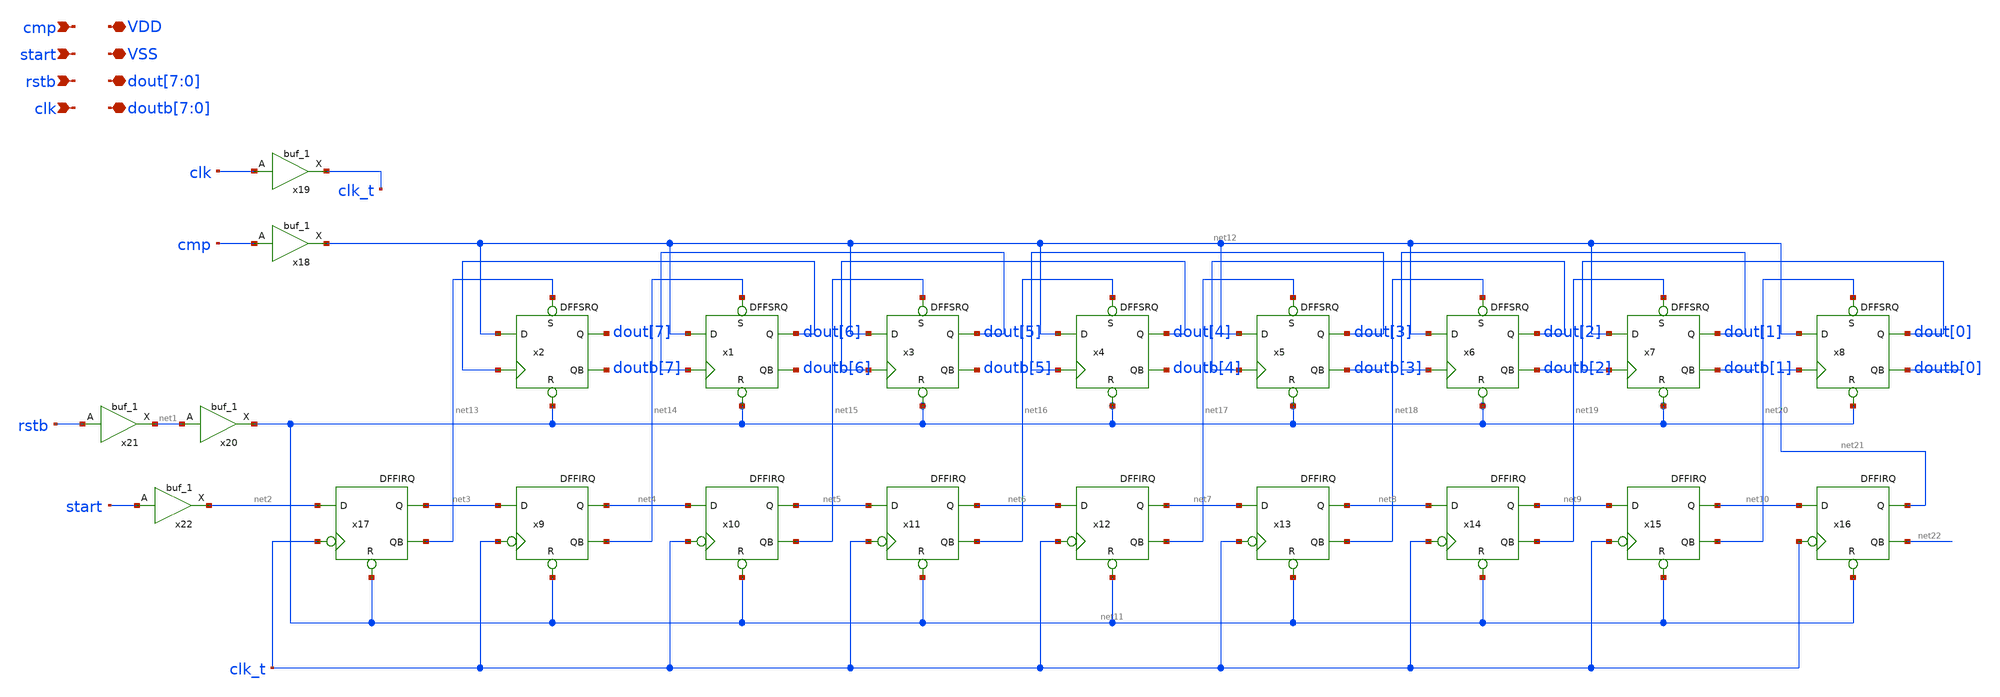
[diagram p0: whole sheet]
** sch_path: 8bitADC_SARLOGIC.sch
**.subckt 8bitADC_SARLOGIC cmp start rstb clk
*+ dout[7],dout[6],dout[5],dout[4],dout[3],dout[2],dout[1],dout[0] doutb[7],doutb[6],doutb[5],doutb[4],doutb[3],doutb[2],doutb[1],doutb[0] VSS VDD
*.ipin cmp
*.ipin start
*.ipin rstb
*.ipin clk
*.iopin dout[7],dout[6],dout[5],dout[4],dout[3],dout[2],dout[1],dout[0]
*.iopin doutb[7],doutb[6],doutb[5],doutb[4],doutb[3],doutb[2],doutb[1],doutb[0]
*.iopin VSS
*.iopin VDD
x2 dout[7] doutb[7] net12 dout[6] net13 net11 VDD VSS VCC VSS DFFSRQ
x1 dout[6] doutb[6] net12 dout[5] net14 net11 VDD VSS VCC VSS DFFSRQ
x3 dout[5] doutb[5] net12 dout[4] net15 net11 VDD VSS VCC VSS DFFSRQ
x4 dout[4] doutb[4] net12 dout[3] net16 net11 VDD VSS VCC VSS DFFSRQ
x5 dout[3] doutb[3] net12 dout[2] net17 net11 VDD VSS VCC VSS DFFSRQ
x6 dout[2] doutb[2] net12 dout[1] net18 net11 VDD VSS VCC VSS DFFSRQ
x7 dout[1] doutb[1] net12 dout[0] net19 net11 VDD VSS VCC VSS DFFSRQ
x8 dout[0] doutb[0] net12 net21 net20 net11 VDD VSS VCC VSS DFFSRQ
x9 net4 net14 net3 clk_t net11 VDD VSS VCC VSS DFFIRQ
x10 net5 net15 net4 clk_t net11 VDD VSS VCC VSS DFFIRQ
x11 net6 net16 net5 clk_t net11 VDD VSS VCC VSS DFFIRQ
x12 net7 net17 net6 clk_t net11 VDD VSS VCC VSS DFFIRQ
x13 net8 net18 net7 clk_t net11 VDD VSS VCC VSS DFFIRQ
x14 net9 net19 net8 clk_t net11 VDD VSS VCC VSS DFFIRQ
x15 net10 net20 net9 clk_t net11 VDD VSS VCC VSS DFFIRQ
x16 net21 net22 net10 clk_t net11 VDD VSS VCC VSS DFFIRQ
x17 net3 net13 net2 clk_t net11 VDD VSS VCC VSS DFFIRQ
x18 cmp VSS VNB VPB VDD net12 sky130_fd_sc_hd__buf_1
x19 clk VSS VNB VPB VDD clk_t sky130_fd_sc_hd__buf_1
x20 net1 VSS VNB VPB VDD net11 sky130_fd_sc_hd__buf_1
x21 rstb VSS VNB VPB VDD net1 sky130_fd_sc_hd__buf_1
x22 start VSS VNB VPB VDD net2 sky130_fd_sc_hd__buf_1
**** begin user architecture code

** opencircuitdesign pdks install
.lib $::SKYWATER_MODELS/sky130.lib.spice tt
.include $::SKYWATER_STDCELLS/sky130_fd_sc_hd.spice


**** end user architecture code
**.ends
.end
